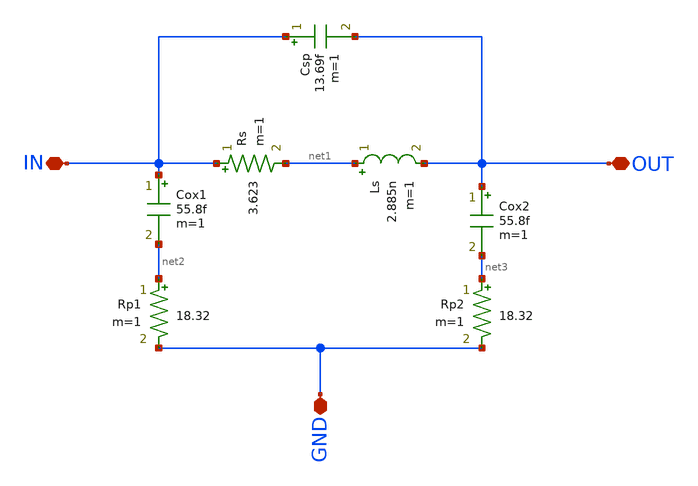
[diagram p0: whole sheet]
** sch_path: Inductance/MODEL_XSCHEM/inductance_3nH.sch
**.subckt inductance_3nH GND OUT IN
*.iopin GND
*.iopin OUT
*.iopin IN
Ls net1 OUT 2.885n m=1
Cox1 IN net2 55.8f m=1
Cox2 OUT net3 55.8f m=1
Csp IN OUT 13.69f m=1
Rp1 net2 GND 18.32 m=1
Rp2 net3 GND 18.32 m=1
Rs IN net1 3.623 m=1
**.ends
.end
